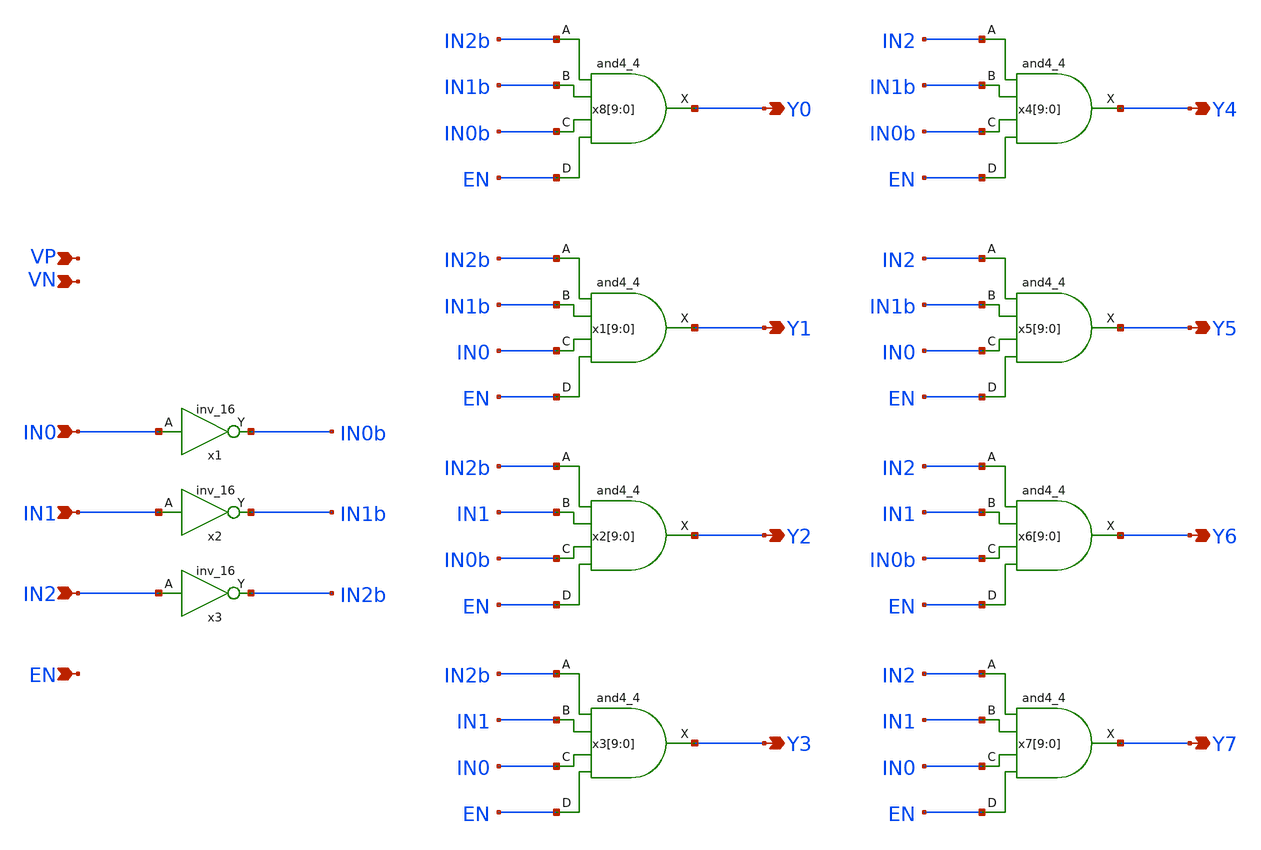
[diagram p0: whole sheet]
** sch_path: xschem/decoder_3to8_top.sch
**.subckt decoder_3to8_top VP VN IN1 IN0 IN2 EN Y0 Y1 Y2 Y3 Y4 Y5 Y6 Y7
*.ipin VP
*.ipin VN
*.ipin IN1
*.ipin IN0
*.ipin IN2
*.ipin EN
*.opin Y0
*.opin Y1
*.opin Y2
*.opin Y3
*.opin Y4
*.opin Y5
*.opin Y6
*.opin Y7
x1 IN0 VN VN VP VP IN0b sky130_fd_sc_hd__inv_16
x2 IN1 VN VN VP VP IN1b sky130_fd_sc_hd__inv_16
x3 IN2 VN VN VP VP IN2b sky130_fd_sc_hd__inv_16
x8[9] IN2b IN1b IN0b EN VN VN VP VP Y0 sky130_fd_sc_hd__and4_4
x8[8] IN2b IN1b IN0b EN VN VN VP VP Y0 sky130_fd_sc_hd__and4_4
x8[7] IN2b IN1b IN0b EN VN VN VP VP Y0 sky130_fd_sc_hd__and4_4
x8[6] IN2b IN1b IN0b EN VN VN VP VP Y0 sky130_fd_sc_hd__and4_4
x8[5] IN2b IN1b IN0b EN VN VN VP VP Y0 sky130_fd_sc_hd__and4_4
x8[4] IN2b IN1b IN0b EN VN VN VP VP Y0 sky130_fd_sc_hd__and4_4
x8[3] IN2b IN1b IN0b EN VN VN VP VP Y0 sky130_fd_sc_hd__and4_4
x8[2] IN2b IN1b IN0b EN VN VN VP VP Y0 sky130_fd_sc_hd__and4_4
x8[1] IN2b IN1b IN0b EN VN VN VP VP Y0 sky130_fd_sc_hd__and4_4
x8[0] IN2b IN1b IN0b EN VN VN VP VP Y0 sky130_fd_sc_hd__and4_4
x1[9] IN2b IN1b IN0 EN VN VN VP VP Y1 sky130_fd_sc_hd__and4_4
x1[8] IN2b IN1b IN0 EN VN VN VP VP Y1 sky130_fd_sc_hd__and4_4
x1[7] IN2b IN1b IN0 EN VN VN VP VP Y1 sky130_fd_sc_hd__and4_4
x1[6] IN2b IN1b IN0 EN VN VN VP VP Y1 sky130_fd_sc_hd__and4_4
x1[5] IN2b IN1b IN0 EN VN VN VP VP Y1 sky130_fd_sc_hd__and4_4
x1[4] IN2b IN1b IN0 EN VN VN VP VP Y1 sky130_fd_sc_hd__and4_4
x1[3] IN2b IN1b IN0 EN VN VN VP VP Y1 sky130_fd_sc_hd__and4_4
x1[2] IN2b IN1b IN0 EN VN VN VP VP Y1 sky130_fd_sc_hd__and4_4
x1[1] IN2b IN1b IN0 EN VN VN VP VP Y1 sky130_fd_sc_hd__and4_4
x1[0] IN2b IN1b IN0 EN VN VN VP VP Y1 sky130_fd_sc_hd__and4_4
x2[9] IN2b IN1 IN0b EN VN VN VP VP Y2 sky130_fd_sc_hd__and4_4
x2[8] IN2b IN1 IN0b EN VN VN VP VP Y2 sky130_fd_sc_hd__and4_4
x2[7] IN2b IN1 IN0b EN VN VN VP VP Y2 sky130_fd_sc_hd__and4_4
x2[6] IN2b IN1 IN0b EN VN VN VP VP Y2 sky130_fd_sc_hd__and4_4
x2[5] IN2b IN1 IN0b EN VN VN VP VP Y2 sky130_fd_sc_hd__and4_4
x2[4] IN2b IN1 IN0b EN VN VN VP VP Y2 sky130_fd_sc_hd__and4_4
x2[3] IN2b IN1 IN0b EN VN VN VP VP Y2 sky130_fd_sc_hd__and4_4
x2[2] IN2b IN1 IN0b EN VN VN VP VP Y2 sky130_fd_sc_hd__and4_4
x2[1] IN2b IN1 IN0b EN VN VN VP VP Y2 sky130_fd_sc_hd__and4_4
x2[0] IN2b IN1 IN0b EN VN VN VP VP Y2 sky130_fd_sc_hd__and4_4
x3[9] IN2b IN1 IN0 EN VN VN VP VP Y3 sky130_fd_sc_hd__and4_4
x3[8] IN2b IN1 IN0 EN VN VN VP VP Y3 sky130_fd_sc_hd__and4_4
x3[7] IN2b IN1 IN0 EN VN VN VP VP Y3 sky130_fd_sc_hd__and4_4
x3[6] IN2b IN1 IN0 EN VN VN VP VP Y3 sky130_fd_sc_hd__and4_4
x3[5] IN2b IN1 IN0 EN VN VN VP VP Y3 sky130_fd_sc_hd__and4_4
x3[4] IN2b IN1 IN0 EN VN VN VP VP Y3 sky130_fd_sc_hd__and4_4
x3[3] IN2b IN1 IN0 EN VN VN VP VP Y3 sky130_fd_sc_hd__and4_4
x3[2] IN2b IN1 IN0 EN VN VN VP VP Y3 sky130_fd_sc_hd__and4_4
x3[1] IN2b IN1 IN0 EN VN VN VP VP Y3 sky130_fd_sc_hd__and4_4
x3[0] IN2b IN1 IN0 EN VN VN VP VP Y3 sky130_fd_sc_hd__and4_4
x4[9] IN2 IN1b IN0b EN VN VN VP VP Y4 sky130_fd_sc_hd__and4_4
x4[8] IN2 IN1b IN0b EN VN VN VP VP Y4 sky130_fd_sc_hd__and4_4
x4[7] IN2 IN1b IN0b EN VN VN VP VP Y4 sky130_fd_sc_hd__and4_4
x4[6] IN2 IN1b IN0b EN VN VN VP VP Y4 sky130_fd_sc_hd__and4_4
x4[5] IN2 IN1b IN0b EN VN VN VP VP Y4 sky130_fd_sc_hd__and4_4
x4[4] IN2 IN1b IN0b EN VN VN VP VP Y4 sky130_fd_sc_hd__and4_4
x4[3] IN2 IN1b IN0b EN VN VN VP VP Y4 sky130_fd_sc_hd__and4_4
x4[2] IN2 IN1b IN0b EN VN VN VP VP Y4 sky130_fd_sc_hd__and4_4
x4[1] IN2 IN1b IN0b EN VN VN VP VP Y4 sky130_fd_sc_hd__and4_4
x4[0] IN2 IN1b IN0b EN VN VN VP VP Y4 sky130_fd_sc_hd__and4_4
x5[9] IN2 IN1b IN0 EN VN VN VP VP Y5 sky130_fd_sc_hd__and4_4
x5[8] IN2 IN1b IN0 EN VN VN VP VP Y5 sky130_fd_sc_hd__and4_4
x5[7] IN2 IN1b IN0 EN VN VN VP VP Y5 sky130_fd_sc_hd__and4_4
x5[6] IN2 IN1b IN0 EN VN VN VP VP Y5 sky130_fd_sc_hd__and4_4
x5[5] IN2 IN1b IN0 EN VN VN VP VP Y5 sky130_fd_sc_hd__and4_4
x5[4] IN2 IN1b IN0 EN VN VN VP VP Y5 sky130_fd_sc_hd__and4_4
x5[3] IN2 IN1b IN0 EN VN VN VP VP Y5 sky130_fd_sc_hd__and4_4
x5[2] IN2 IN1b IN0 EN VN VN VP VP Y5 sky130_fd_sc_hd__and4_4
x5[1] IN2 IN1b IN0 EN VN VN VP VP Y5 sky130_fd_sc_hd__and4_4
x5[0] IN2 IN1b IN0 EN VN VN VP VP Y5 sky130_fd_sc_hd__and4_4
x6[9] IN2 IN1 IN0b EN VN VN VP VP Y6 sky130_fd_sc_hd__and4_4
x6[8] IN2 IN1 IN0b EN VN VN VP VP Y6 sky130_fd_sc_hd__and4_4
x6[7] IN2 IN1 IN0b EN VN VN VP VP Y6 sky130_fd_sc_hd__and4_4
x6[6] IN2 IN1 IN0b EN VN VN VP VP Y6 sky130_fd_sc_hd__and4_4
x6[5] IN2 IN1 IN0b EN VN VN VP VP Y6 sky130_fd_sc_hd__and4_4
x6[4] IN2 IN1 IN0b EN VN VN VP VP Y6 sky130_fd_sc_hd__and4_4
x6[3] IN2 IN1 IN0b EN VN VN VP VP Y6 sky130_fd_sc_hd__and4_4
x6[2] IN2 IN1 IN0b EN VN VN VP VP Y6 sky130_fd_sc_hd__and4_4
x6[1] IN2 IN1 IN0b EN VN VN VP VP Y6 sky130_fd_sc_hd__and4_4
x6[0] IN2 IN1 IN0b EN VN VN VP VP Y6 sky130_fd_sc_hd__and4_4
x7[9] IN2 IN1 IN0 EN VN VN VP VP Y7 sky130_fd_sc_hd__and4_4
x7[8] IN2 IN1 IN0 EN VN VN VP VP Y7 sky130_fd_sc_hd__and4_4
x7[7] IN2 IN1 IN0 EN VN VN VP VP Y7 sky130_fd_sc_hd__and4_4
x7[6] IN2 IN1 IN0 EN VN VN VP VP Y7 sky130_fd_sc_hd__and4_4
x7[5] IN2 IN1 IN0 EN VN VN VP VP Y7 sky130_fd_sc_hd__and4_4
x7[4] IN2 IN1 IN0 EN VN VN VP VP Y7 sky130_fd_sc_hd__and4_4
x7[3] IN2 IN1 IN0 EN VN VN VP VP Y7 sky130_fd_sc_hd__and4_4
x7[2] IN2 IN1 IN0 EN VN VN VP VP Y7 sky130_fd_sc_hd__and4_4
x7[1] IN2 IN1 IN0 EN VN VN VP VP Y7 sky130_fd_sc_hd__and4_4
x7[0] IN2 IN1 IN0 EN VN VN VP VP Y7 sky130_fd_sc_hd__and4_4
**** begin user architecture code
 .lib $::SKYWATER_MODELS/sky130.lib.spice tt
.include $::SKYWATER_STDCELLS/sky130_fd_sc_hd.spice

**** end user architecture code
**.ends
.end
